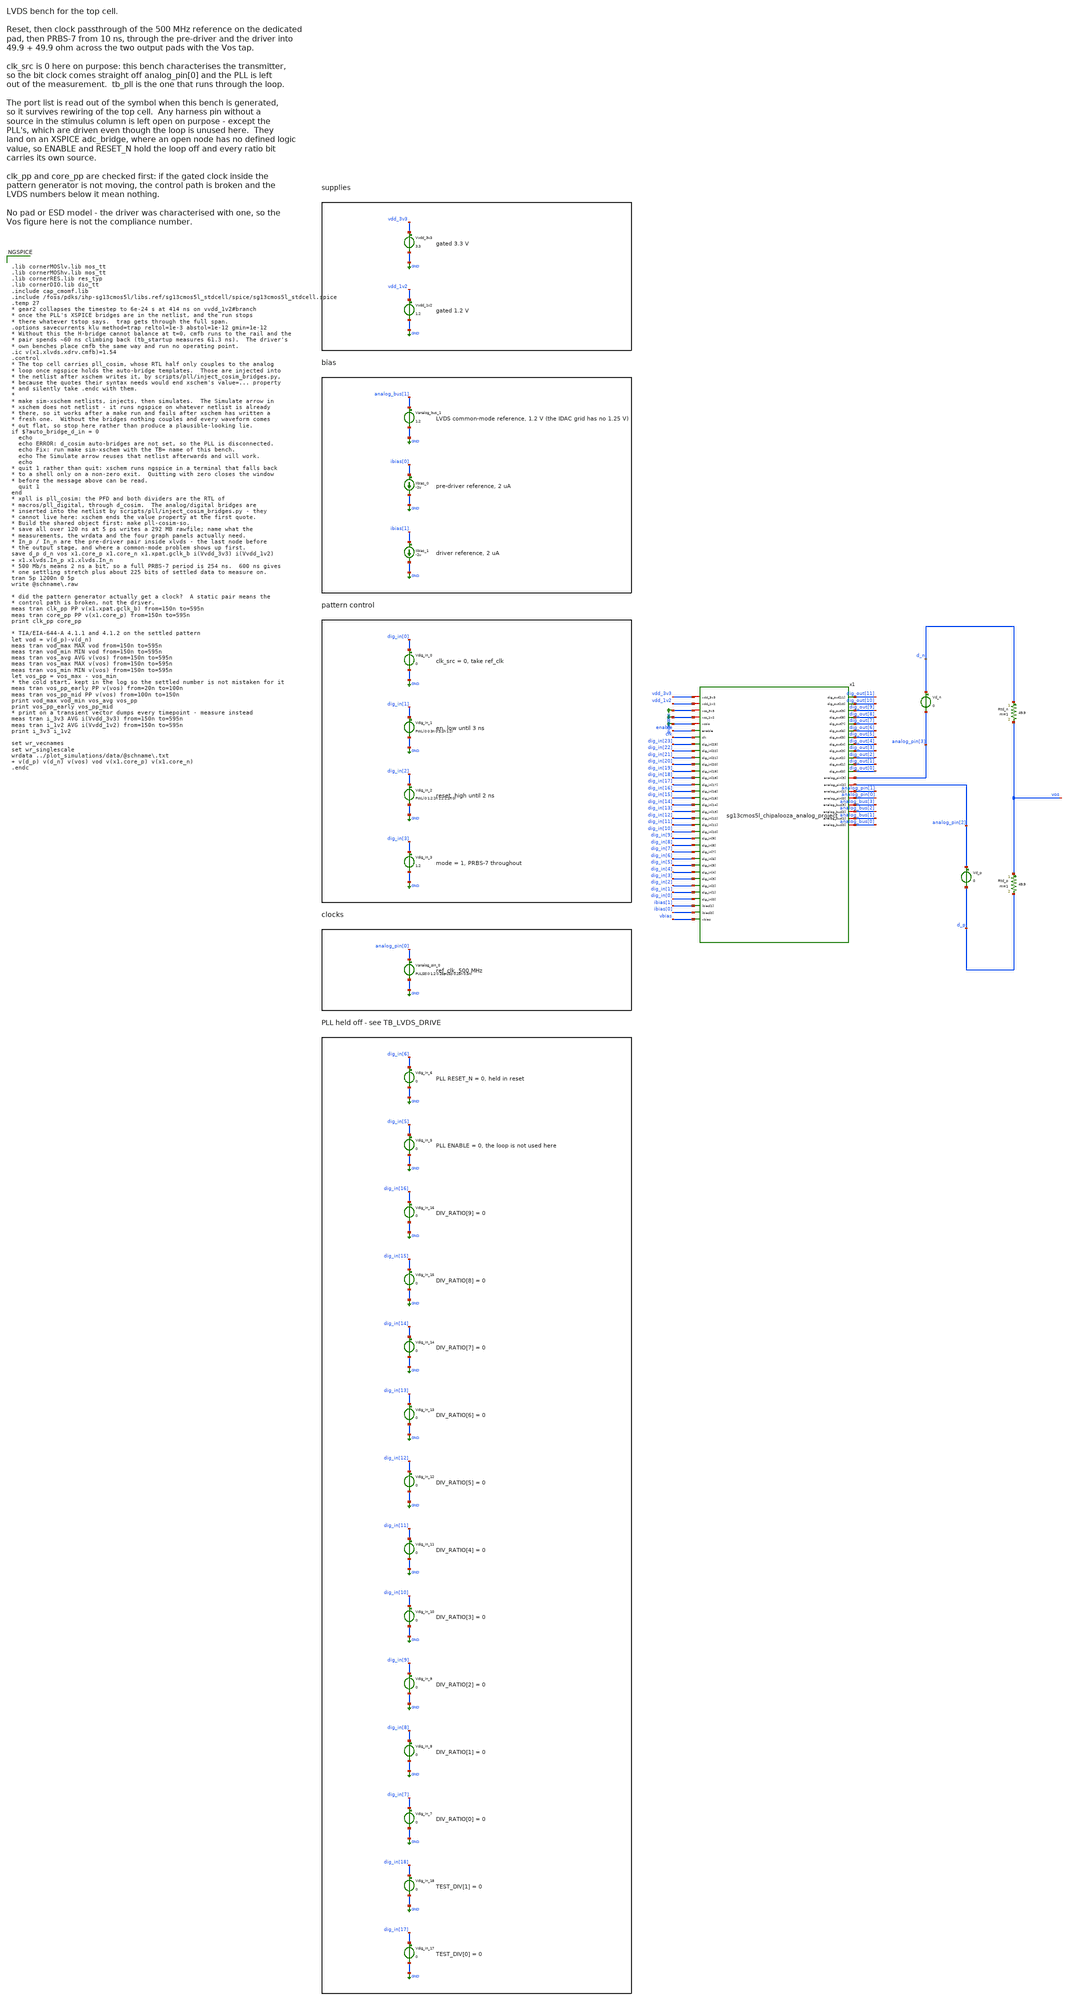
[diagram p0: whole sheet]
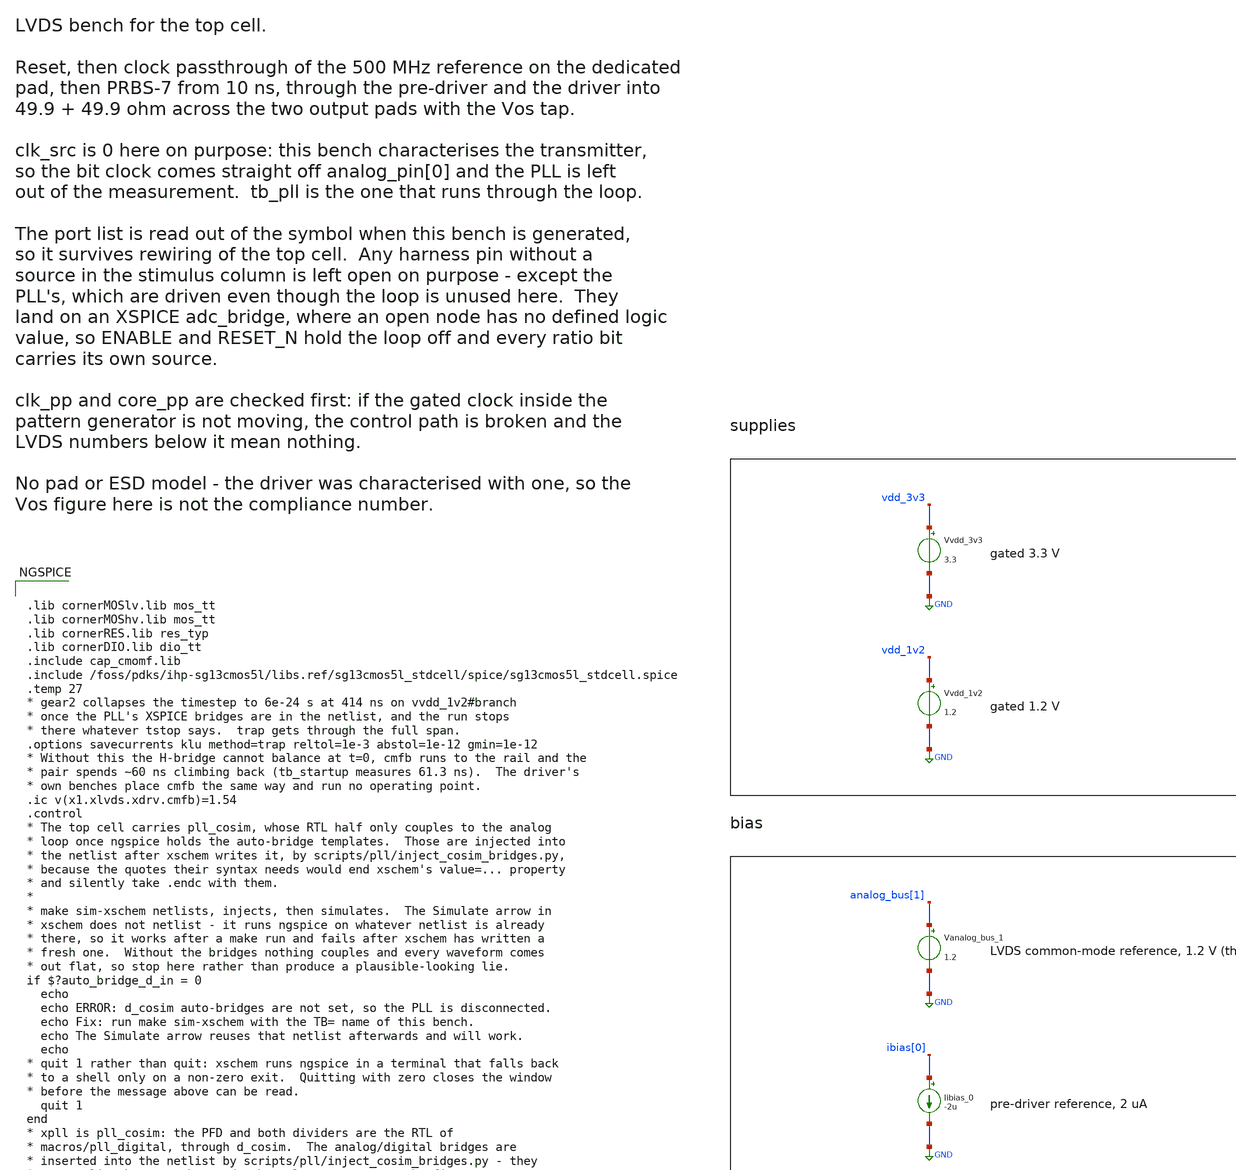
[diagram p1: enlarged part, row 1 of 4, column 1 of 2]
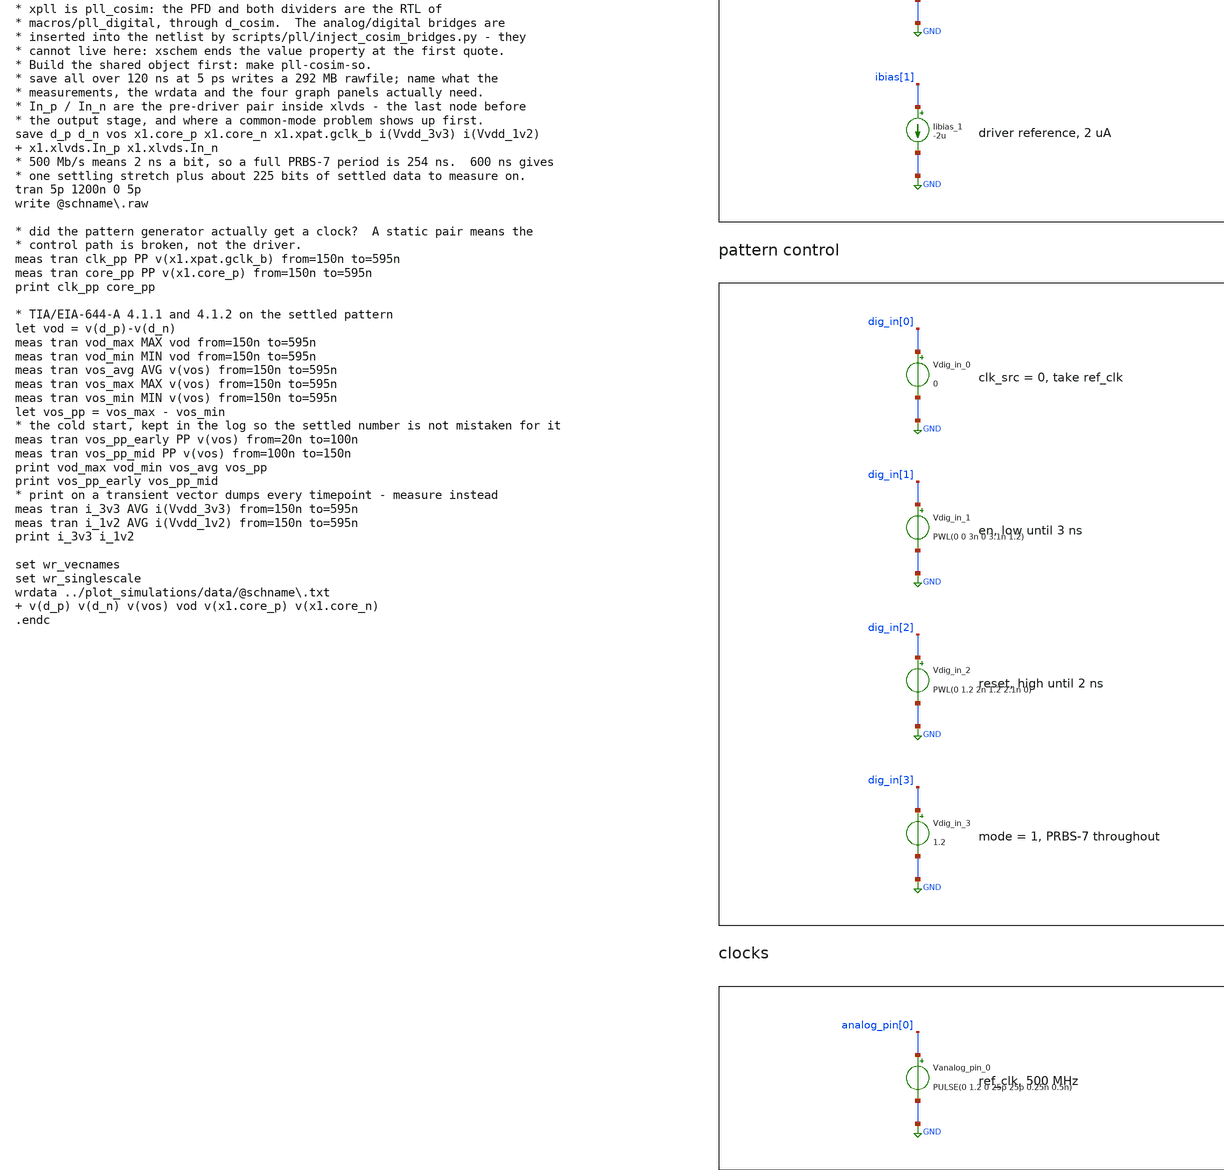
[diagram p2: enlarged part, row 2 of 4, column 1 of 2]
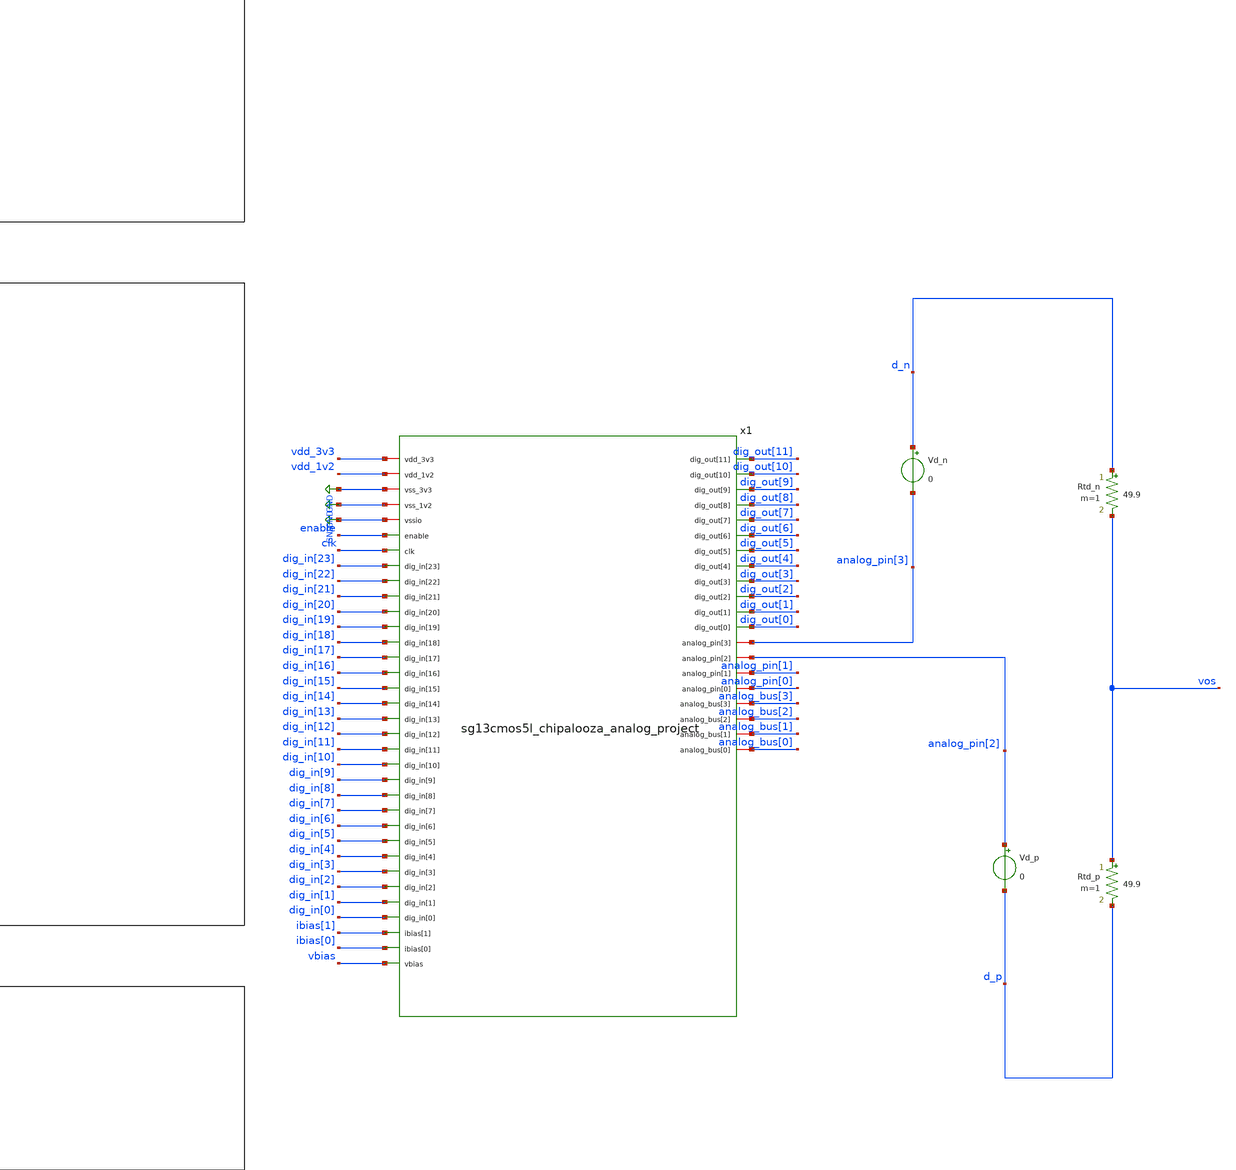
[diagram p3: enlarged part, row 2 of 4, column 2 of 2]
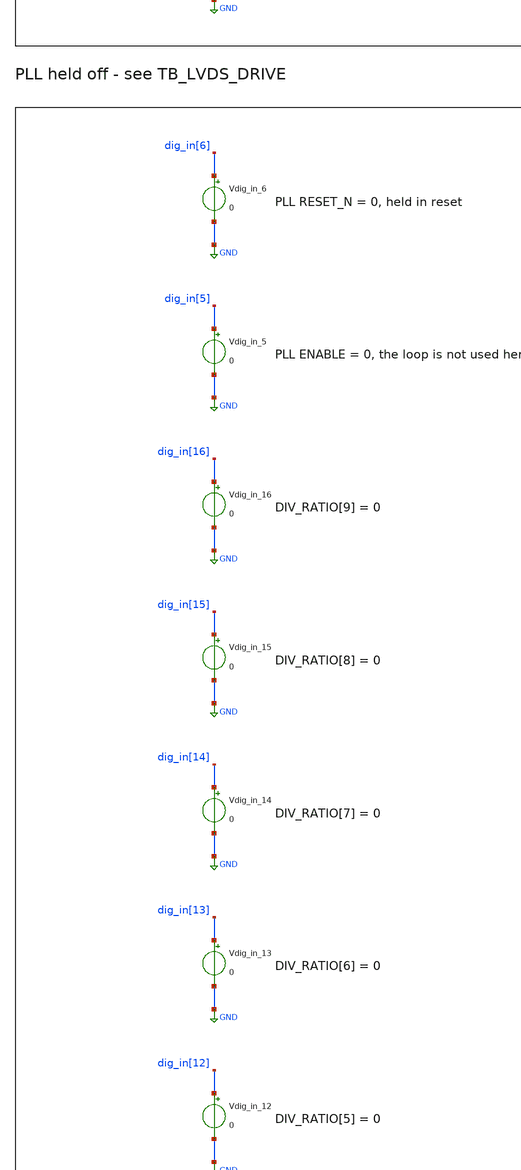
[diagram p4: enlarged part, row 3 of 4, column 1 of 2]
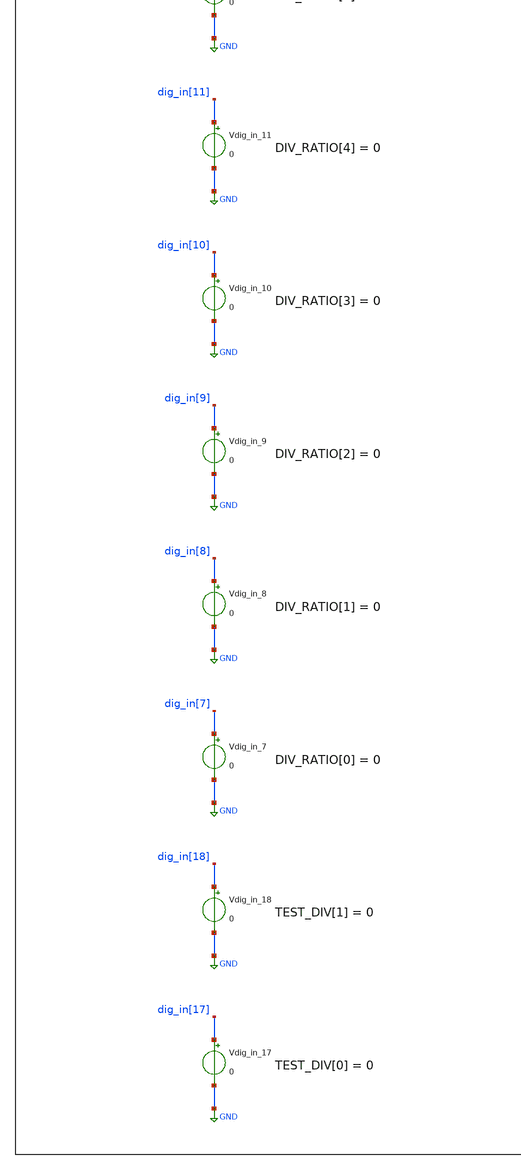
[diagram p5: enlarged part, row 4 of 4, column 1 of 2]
** sch_path: testbenches/xschem/sg13cmos5l_chipalooza_analog_project_tb_lvds.sch
**.subckt sg13cmos5l_chipalooza_analog_project_tb_lvds
Vvdd_3v3 vdd_3v3 GND 3.3
Vvdd_1v2 vdd_1v2 GND 1.2
Vanalog_bus_1 analog_bus[1] GND 1.2
Iibias_0 ibias[0] GND -2u
Iibias_1 ibias[1] GND -2u
Vdig_in_0 dig_in[0] GND 0
Vdig_in_1 dig_in[1] GND PWL(0 0 3n 0 3.1n 1.2)
Vdig_in_2 dig_in[2] GND PWL(0 1.2 2n 1.2 2.1n 0)
Vdig_in_3 dig_in[3] GND 1.2
Vanalog_pin_0 analog_pin[0] GND PULSE(0 1.2 0 25p 25p 0.25n 0.5n)
Vdig_in_6 dig_in[6] GND 0
Vdig_in_5 dig_in[5] GND 0
Vdig_in_16 dig_in[16] GND 0
Vdig_in_15 dig_in[15] GND 0
Vdig_in_14 dig_in[14] GND 0
Vdig_in_13 dig_in[13] GND 0
Vdig_in_12 dig_in[12] GND 0
Vdig_in_11 dig_in[11] GND 0
Vdig_in_10 dig_in[10] GND 0
Vdig_in_9 dig_in[9] GND 0
Vdig_in_8 dig_in[8] GND 0
Vdig_in_7 dig_in[7] GND 0
Vdig_in_18 dig_in[18] GND 0
Vdig_in_17 dig_in[17] GND 0
x1 vdd_3v3 vdd_1v2 GND GND GND enable clk dig_in[23] dig_in[22] dig_in[21] dig_in[20] dig_in[19]
+ dig_in[18] dig_in[17] dig_in[16] dig_in[15] dig_in[14] dig_in[13] dig_in[12] dig_in[11] dig_in[10] dig_in[9]
+ dig_in[8] dig_in[7] dig_in[6] dig_in[5] dig_in[4] dig_in[3] dig_in[2] dig_in[1] dig_in[0] ibias[1] ibias[0]
+ vbias dig_out[11] dig_out[10] dig_out[9] dig_out[8] dig_out[7] dig_out[6] dig_out[5] dig_out[4]
+ dig_out[3] dig_out[2] dig_out[1] dig_out[0] analog_pin[3] analog_pin[2] analog_pin[1] analog_pin[0]
+ analog_bus[3] analog_bus[2] analog_bus[1] analog_bus[0] sg13cmos5l_chipalooza_analog_project
Vd_n d_n analog_pin[3] 0
Vd_p analog_pin[2] d_p 0
Rtd_n d_n vos 49.9 m=1
Rtd_p vos d_p 49.9 m=1
**** begin user architecture code


.lib cornerMOSlv.lib mos_tt
.lib cornerMOShv.lib mos_tt
.lib cornerRES.lib res_typ
.lib cornerDIO.lib dio_tt
.include cap_cmomf.lib
.include /foss/pdks/ihp-sg13cmos5l/libs.ref/sg13cmos5l_stdcell/spice/sg13cmos5l_stdcell.spice
.temp 27
* gear2 collapses the timestep to 6e-24 s at 414 ns on vvdd_1v2#branch
* once the PLL's XSPICE bridges are in the netlist, and the run stops
* there whatever tstop says.  trap gets through the full span.
.options savecurrents klu method=trap reltol=1e-3 abstol=1e-12 gmin=1e-12
* Without this the H-bridge cannot balance at t=0, cmfb runs to the rail and the
* pair spends ~60 ns climbing back (tb_startup measures 61.3 ns).  The driver's
* own benches place cmfb the same way and run no operating point.
.ic v(x1.xlvds.xdrv.cmfb)=1.54
.control
* The top cell carries pll_cosim, whose RTL half only couples to the analog
* loop once ngspice holds the auto-bridge templates.  Those are injected into
* the netlist after xschem writes it, by scripts/pll/inject_cosim_bridges.py,
* because the quotes their syntax needs would end xschem's value=... property
* and silently take .endc with them.
*
* make sim-xschem netlists, injects, then simulates.  The Simulate arrow in
* xschem does not netlist - it runs ngspice on whatever netlist is already
* there, so it works after a make run and fails after xschem has written a
* fresh one.  Without the bridges nothing couples and every waveform comes
* out flat, so stop here rather than produce a plausible-looking lie.
if $?auto_bridge_d_in = 0
  echo
  echo ERROR: d_cosim auto-bridges are not set, so the PLL is disconnected.
  echo Fix: run make sim-xschem with the TB= name of this bench.
  echo The Simulate arrow reuses that netlist afterwards and will work.
  echo
* quit 1 rather than quit: xschem runs ngspice in a terminal that falls back
* to a shell only on a non-zero exit.  Quitting with zero closes the window
* before the message above can be read.
  quit 1
end
* xpll is pll_cosim: the PFD and both dividers are the RTL of
* macros/pll_digital, through d_cosim.  The analog/digital bridges are
* inserted into the netlist by scripts/pll/inject_cosim_bridges.py - they
* cannot live here: xschem ends the value property at the first quote.
* Build the shared object first: make pll-cosim-so.
* save all over 120 ns at 5 ps writes a 292 MB rawfile; name what the
* measurements, the wrdata and the four graph panels actually need.
* In_p / In_n are the pre-driver pair inside xlvds - the last node before
* the output stage, and where a common-mode problem shows up first.
save d_p d_n vos x1.core_p x1.core_n x1.xpat.gclk_b i(Vvdd_3v3) i(Vvdd_1v2)  x1.xlvds.In_p x1.xlvds.In_n
* 500 Mb/s means 2 ns a bit, so a full PRBS-7 period is 254 ns.  600 ns gives
* one settling stretch plus about 225 bits of settled data to measure on.
tran 5p 1200n 0 5p
write @schname\.raw

* did the pattern generator actually get a clock?  A static pair means the
* control path is broken, not the driver.
meas tran clk_pp PP v(x1.xpat.gclk_b) from=150n to=595n
meas tran core_pp PP v(x1.core_p) from=150n to=595n
print clk_pp core_pp

* TIA/EIA-644-A 4.1.1 and 4.1.2 on the settled pattern
let vod = v(d_p)-v(d_n)
meas tran vod_max MAX vod from=150n to=595n
meas tran vod_min MIN vod from=150n to=595n
meas tran vos_avg AVG v(vos) from=150n to=595n
meas tran vos_max MAX v(vos) from=150n to=595n
meas tran vos_min MIN v(vos) from=150n to=595n
let vos_pp = vos_max - vos_min
* the cold start, kept in the log so the settled number is not mistaken for it
meas tran vos_pp_early PP v(vos) from=20n to=100n
meas tran vos_pp_mid PP v(vos) from=100n to=150n
print vod_max vod_min vos_avg vos_pp
print vos_pp_early vos_pp_mid
* print on a transient vector dumps every timepoint - measure instead
meas tran i_3v3 AVG i(Vvdd_3v3) from=150n to=595n
meas tran i_1v2 AVG i(Vvdd_1v2) from=150n to=595n
print i_3v3 i_1v2

set wr_vecnames
set wr_singlescale
wrdata ../plot_simulations/data/@schname\.txt  v(d_p) v(d_n) v(vos) vod v(x1.core_p) v(x1.core_n)
.endc


**** end user architecture code
**.ends
.GLOBAL GND
.end
